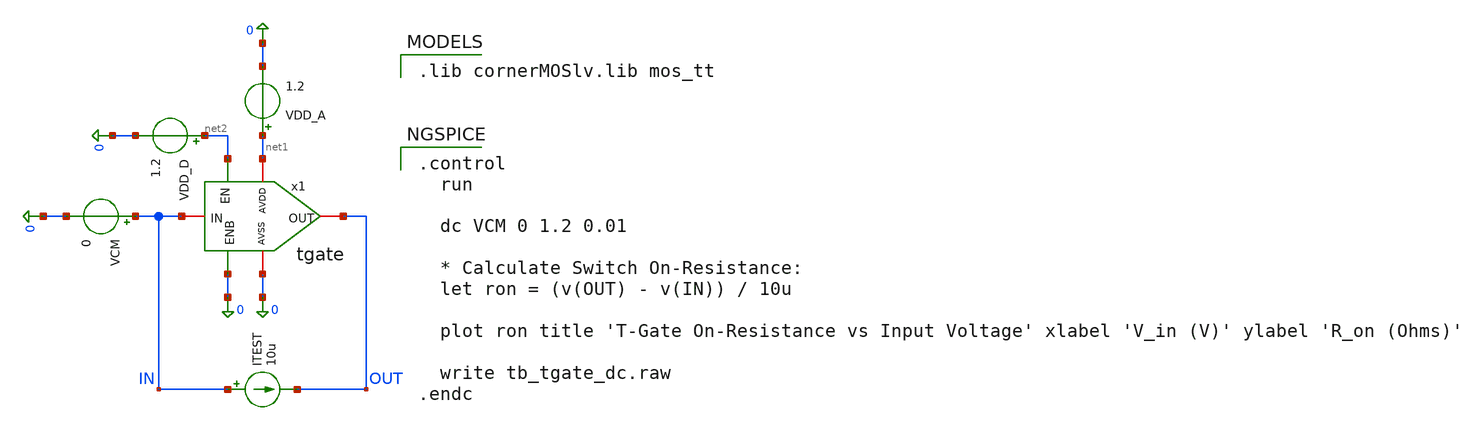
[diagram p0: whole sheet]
** sch_path: designs/libs/core_digital/tgate/tb_tgate.sch
**.subckt tb_tgate
x1 IN 0 net1 net2 0 OUT tgate
ITEST IN OUT 10u
VDD_A net1 0 1.2
VCM IN 0 0
VDD_D net2 0 1.2
**** begin user architecture code

.lib cornerMOSlv.lib mos_tt


.control
  run

  dc VCM 0 1.2 0.01

  * Calculate Switch On-Resistance:
  let ron = (v(OUT) - v(IN)) / 10u

  plot ron title 'T-Gate On-Resistance vs Input Voltage' xlabel 'V_in (V)' ylabel 'R_on (Ohms)'

  write tb_tgate_dc.raw
.endc



**** end user architecture code
**.ends

* expanding   symbol:  tgate.sym # of pins=6
** sym_path: designs/libs/core_digital/tgate/tgate.sym
** sch_path: designs/libs/core_digital/tgate/tgate.sch
.subckt tgate IN AVSS AVDD EN ENB OUT
*.iopin AVDD
*.iopin AVSS
*.iopin IN
*.iopin OUT
*.ipin EN
*.ipin ENB
XM1 IN EN OUT AVSS sg13_lv_nmos w=1u l=0.13u ng=1 m=1 mm_ok=1
XM2 OUT ENB IN AVDD sg13_lv_pmos w=2.5u l=0.13u ng=1 m=1 mm_ok=1
.ends

.end
